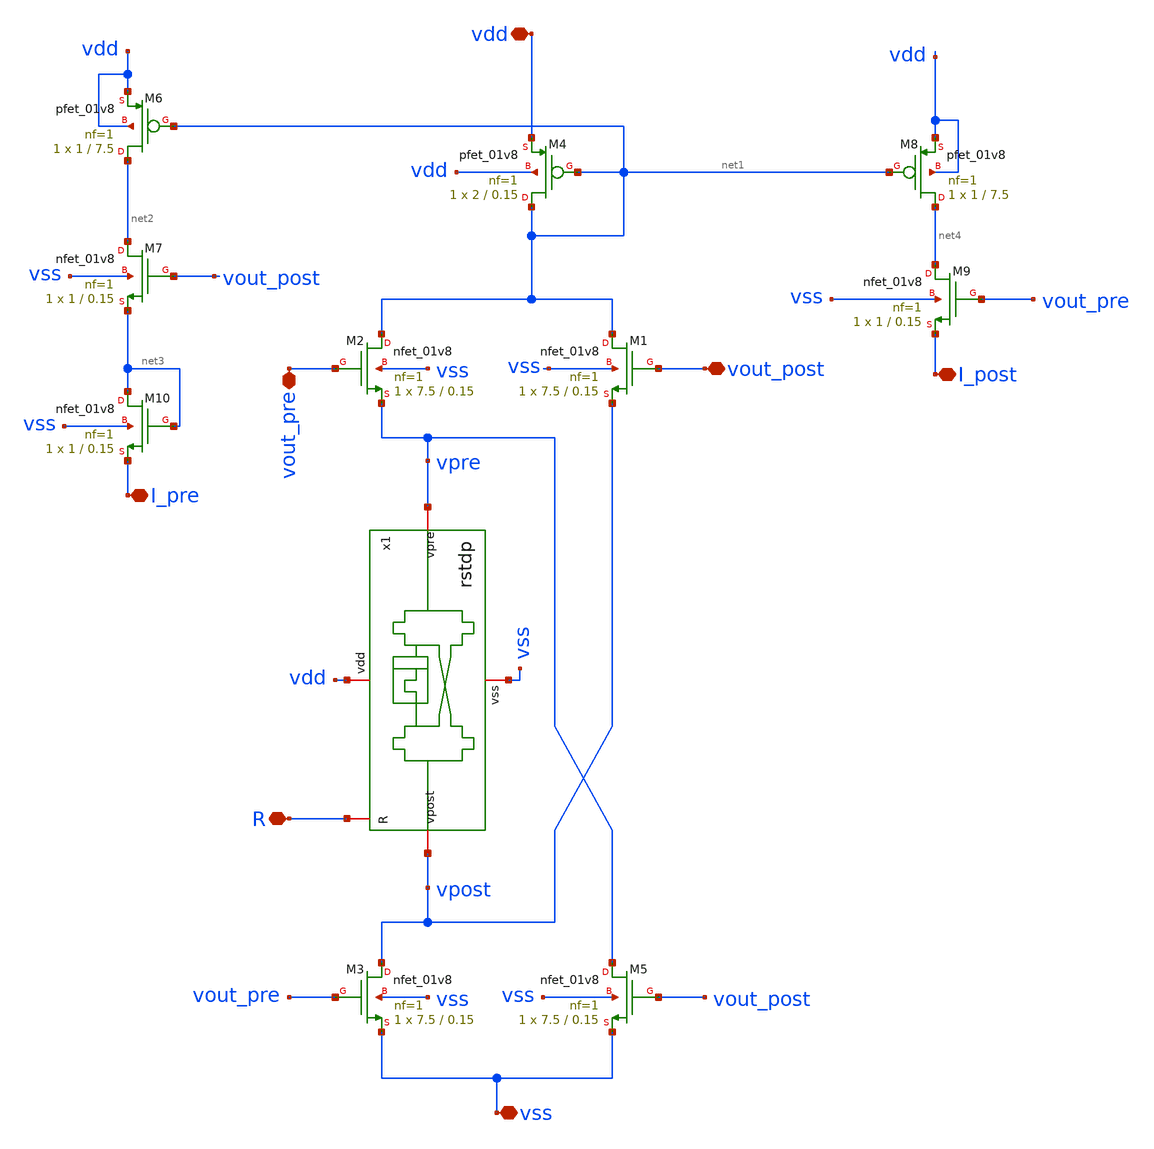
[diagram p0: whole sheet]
** sch_path: Synapse/rstdp_mirror.sch
**.subckt rstdp_mirror vdd vss R vout_post vout_pre I_post I_pre
*.iopin vdd
*.iopin vss
*.iopin R
*.iopin vout_post
*.iopin vout_pre
*.iopin I_post
*.iopin I_pre
XM2 net1 vout_pre vpre vss sky130_fd_pr__nfet_01v8 L=0.15 W=7.5 nf=1 ad='int((nf+1)/2) * W/nf * 0.29'
+ as='int((nf+2)/2) * W/nf * 0.29' pd='2*int((nf+1)/2) * (W/nf + 0.29)' ps='2*int((nf+2)/2) * (W/nf + 0.29)'
+ nrd='0.29 / W' nrs='0.29 / W' sa=0 sb=0 sd=0 mult=1 m=1
XM3 vpost vout_pre vss vss sky130_fd_pr__nfet_01v8 L=0.15 W=7.5 nf=1 ad='int((nf+1)/2) * W/nf * 0.29'
+ as='int((nf+2)/2) * W/nf * 0.29' pd='2*int((nf+1)/2) * (W/nf + 0.29)' ps='2*int((nf+2)/2) * (W/nf + 0.29)'
+ nrd='0.29 / W' nrs='0.29 / W' sa=0 sb=0 sd=0 mult=1 m=1
x1 R vdd vss vpost vpre rstdp
XM1 net1 vout_post vpost vss sky130_fd_pr__nfet_01v8 L=0.15 W=7.5 nf=1 ad='int((nf+1)/2) * W/nf * 0.29'
+ as='int((nf+2)/2) * W/nf * 0.29' pd='2*int((nf+1)/2) * (W/nf + 0.29)' ps='2*int((nf+2)/2) * (W/nf + 0.29)'
+ nrd='0.29 / W' nrs='0.29 / W' sa=0 sb=0 sd=0 mult=1 m=1
XM5 vpre vout_post vss vss sky130_fd_pr__nfet_01v8 L=0.15 W=7.5 nf=1 ad='int((nf+1)/2) * W/nf * 0.29'
+ as='int((nf+2)/2) * W/nf * 0.29' pd='2*int((nf+1)/2) * (W/nf + 0.29)' ps='2*int((nf+2)/2) * (W/nf + 0.29)'
+ nrd='0.29 / W' nrs='0.29 / W' sa=0 sb=0 sd=0 mult=1 m=1
XM4 net1 net1 vdd vdd sky130_fd_pr__pfet_01v8 L=0.15 W=2 nf=1 ad='int((nf+1)/2) * W/nf * 0.29' as='int((nf+2)/2) * W/nf * 0.29'
+ pd='2*int((nf+1)/2) * (W/nf + 0.29)' ps='2*int((nf+2)/2) * (W/nf + 0.29)' nrd='0.29 / W' nrs='0.29 / W'
+ sa=0 sb=0 sd=0 mult=1 m=1
XM6 net2 net1 vdd vdd sky130_fd_pr__pfet_01v8 L=7.5 W=1 nf=1 ad='int((nf+1)/2) * W/nf * 0.29' as='int((nf+2)/2) * W/nf * 0.29'
+ pd='2*int((nf+1)/2) * (W/nf + 0.29)' ps='2*int((nf+2)/2) * (W/nf + 0.29)' nrd='0.29 / W' nrs='0.29 / W'
+ sa=0 sb=0 sd=0 mult=1 m=1
XM7 net2 vout_post net3 vss sky130_fd_pr__nfet_01v8 L=0.15 W=1 nf=1 ad='int((nf+1)/2) * W/nf * 0.29'
+ as='int((nf+2)/2) * W/nf * 0.29' pd='2*int((nf+1)/2) * (W/nf + 0.29)' ps='2*int((nf+2)/2) * (W/nf + 0.29)'
+ nrd='0.29 / W' nrs='0.29 / W' sa=0 sb=0 sd=0 mult=1 m=1
XM8 net4 net1 vdd vdd sky130_fd_pr__pfet_01v8 L=7.5 W=1 nf=1 ad='int((nf+1)/2) * W/nf * 0.29' as='int((nf+2)/2) * W/nf * 0.29'
+ pd='2*int((nf+1)/2) * (W/nf + 0.29)' ps='2*int((nf+2)/2) * (W/nf + 0.29)' nrd='0.29 / W' nrs='0.29 / W'
+ sa=0 sb=0 sd=0 mult=1 m=1
XM9 net4 vout_pre I_post vss sky130_fd_pr__nfet_01v8 L=0.15 W=1 nf=1 ad='int((nf+1)/2) * W/nf * 0.29'
+ as='int((nf+2)/2) * W/nf * 0.29' pd='2*int((nf+1)/2) * (W/nf + 0.29)' ps='2*int((nf+2)/2) * (W/nf + 0.29)'
+ nrd='0.29 / W' nrs='0.29 / W' sa=0 sb=0 sd=0 mult=1 m=1
XM10 net3 net3 I_pre vss sky130_fd_pr__nfet_01v8 L=0.15 W=1 nf=1 ad='int((nf+1)/2) * W/nf * 0.29' as='int((nf+2)/2) * W/nf * 0.29'
+ pd='2*int((nf+1)/2) * (W/nf + 0.29)' ps='2*int((nf+2)/2) * (W/nf + 0.29)' nrd='0.29 / W' nrs='0.29 / W'
+ sa=0 sb=0 sd=0 mult=1 m=1
**.ends

* expanding   symbol:  /home/alex/Desktop/EDA/SNN_IPN/Synapse/rstdp.sym # of pins=5
** sym_path: Synapse/rstdp.sym
** sch_path: Synapse/rstdp.sch
.subckt rstdp R vdd vss vpost vpre
*.iopin vdd
*.iopin vss
*.iopin R
*.iopin vpre
*.iopin vpost
XR2 te be rram_v0
XM2 vpre R be vss sky130_fd_pr__nfet_01v8 L=0.15 W=7.5 nf=1 ad='int((nf+1)/2) * W/nf * 0.29' as='int((nf+2)/2) * W/nf * 0.29'
+ pd='2*int((nf+1)/2) * (W/nf + 0.29)' ps='2*int((nf+2)/2) * (W/nf + 0.29)' nrd='0.29 / W' nrs='0.29 / W'
+ sa=0 sb=0 sd=0 mult=1 m=1
XM3 te R vpost vss sky130_fd_pr__nfet_01v8 L=0.15 W=7.5 nf=1 ad='int((nf+1)/2) * W/nf * 0.29' as='int((nf+2)/2) * W/nf * 0.29'
+ pd='2*int((nf+1)/2) * (W/nf + 0.29)' ps='2*int((nf+2)/2) * (W/nf + 0.29)' nrd='0.29 / W' nrs='0.29 / W'
+ sa=0 sb=0 sd=0 mult=1 m=1
XM1 te R vpre vdd sky130_fd_pr__pfet_01v8 L=0.15 W=15 nf=1 ad='int((nf+1)/2) * W/nf * 0.29' as='int((nf+2)/2) * W/nf * 0.29'
+ pd='2*int((nf+1)/2) * (W/nf + 0.29)' ps='2*int((nf+2)/2) * (W/nf + 0.29)' nrd='0.29 / W' nrs='0.29 / W'
+ sa=0 sb=0 sd=0 mult=2 m=2
XM4 vpost R be vdd sky130_fd_pr__pfet_01v8 L=0.15 W=15 nf=1 ad='int((nf+1)/2) * W/nf * 0.29' as='int((nf+2)/2) * W/nf * 0.29'
+ pd='2*int((nf+1)/2) * (W/nf + 0.29)' ps='2*int((nf+2)/2) * (W/nf + 0.29)' nrd='0.29 / W' nrs='0.29 / W'
+ sa=0 sb=0 sd=0 mult=2 m=2
.ends

.end
